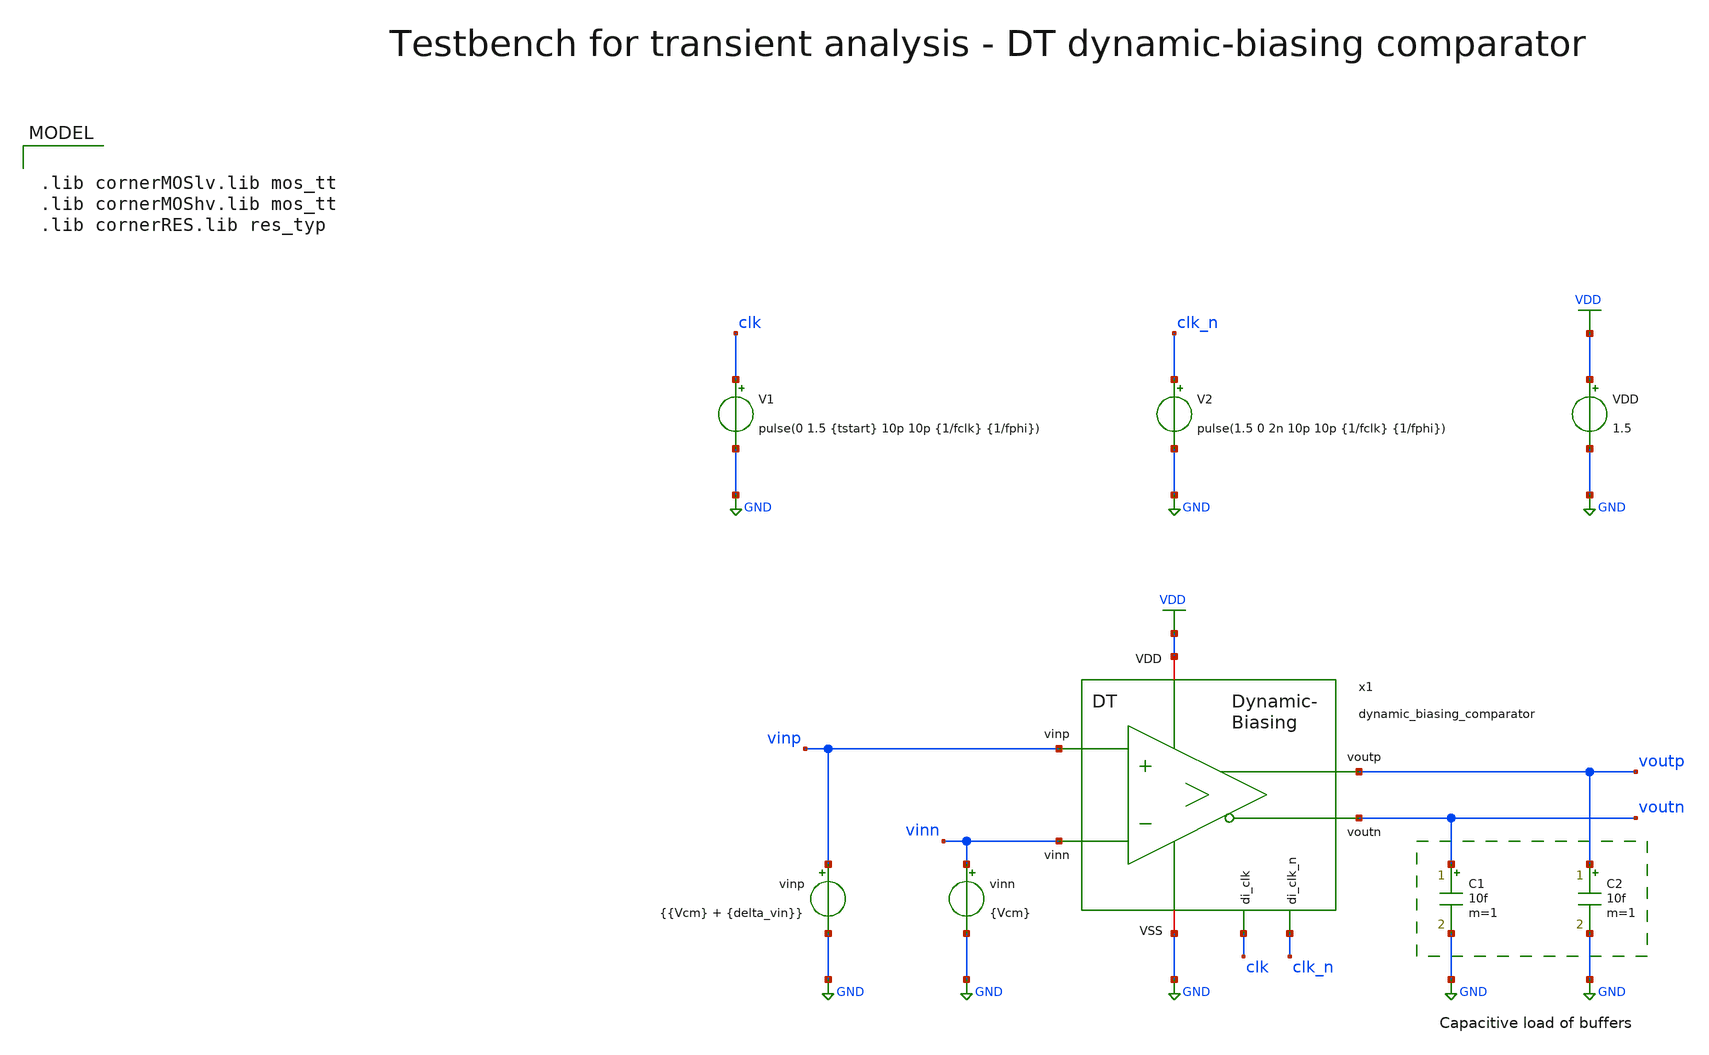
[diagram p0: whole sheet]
** sch_path: SG13G2_ATBS-ADC-main/xschem/comparator/discrete_time/Dynamic-biasing/testbenches/dynamic_biasing_comparator_tb_tran.sch
**.subckt dynamic_biasing_comparator_tb_tran
VDD VDD GND 1.5
V1 clk GND pulse(0 1.5 {tstart} 10p 10p {1/fclk} {1/fphi})
vinn vinn GND {Vcm}
vinp vinp GND {{Vcm} + {delta_vin}}
V2 clk_n GND pulse(1.5 0 2n 10p 10p {1/fclk} {1/fphi})
C1 voutn GND 10f m=1
C2 voutp GND 10f m=1
x1 clk_n clk VDD voutp vinp GND voutn vinn dynamic_biasing_comparator
**** begin user architecture code

.lib cornerMOSlv.lib mos_tt
.lib cornerMOShv.lib mos_tt
.lib cornerRES.lib res_typ



.param temp=27
.param fclk=8000000
.param fphi=62500
.param tstart=2n
.param delta_vin = 10m
.param Vcm=0.75
.csparam fclk=fclk
.csparam tstart=tstart
.options savecurrents reltol=1e-3 abstol=1e-12 gmin=1e-15
.control
save all

* Operating Point Analysis
op
remzerovec
write dynamic_biasing_comparator_tb_tran.raw
set appendwrite

* Transient Analysis
* tran 4p 20n
tran 40p 150n
write dynamic_biasing_comparator_tb_tran.raw

* Measure vcpp_min & vcpn_min
let tmeas = 1/fclk
meas tran vcpp_min FIND v(x1.vcpp) at=tmeas
meas tran vcpn_min FIND v(x1.vcpn) at=tmeas

* Measure Propagation Delay
* Time from clock rising edge to 90% VDD of voutp
let voutp_limit = 0.9 * 1.5
meas tran tcross WHEN v(voutp)=voutp_limit CROSS=1
let tpd = tcross - tstart
echo Propagation Delay $&tpd s

* Calculate Energy / Conversion
* i_int in As
* energy_conv in Ws = J
let N = 1
let t_conv = 150n
meas tran i_int INTEG i(VDD) from=tstart to=t_conv
let energy_conv = 1.5 * i_int / N

let energy_conv_femto = energy_conv * 1e15
echo Energy / Conversion $&energy_conv_femto fJ/conv

* Plotting
plot v(clk) v(x1.vs) v(x1.vctail) v(x1.vcpp) v(x1.vcpn) v(voutp) v(voutn)
plot i(VDD)

* Writing Data
set wr_singlescale
set wr_vecnames
let vs=x1.vs
let vctail=x1.vctail
let vcpp=x1.vcpp
let vcpn=x1.vcpn
wrdata
+ /foss/designs/SG13G2_ATBS-ADC-main/python/plot_simulations/data/dynamic_biasing_comparator_tb_tran.txt v(clk) v(vs) v(vctail) v(vcpp) v(vcpn) v(voutp) v(voutn)

*quit
.endc

**** end user architecture code
**.ends

* expanding   symbol:  comparator/discrete_time/Dynamic-biasing/dynamic_biasing_comparator.sym # of
*+ pins=8
** sym_path: SG13G2_ATBS-ADC-main/xschem/comparator/discrete_time/Dynamic-biasing/dynamic_biasing_comparator.sym
** sch_path: SG13G2_ATBS-ADC-main/xschem/comparator/discrete_time/Dynamic-biasing/dynamic_biasing_comparator.sch
.subckt dynamic_biasing_comparator di_clk_n di_clk VDD voutp vinp VSS voutn vinn
*.iopin VDD
*.opin voutp
*.opin voutn
*.ipin di_clk_n
*.iopin VSS
*.ipin vinp
*.ipin vinn
*.ipin di_clk
XM3a vs di_clk vctail VSS sg13_lv_nmos w=1.0u l=0.13u ng=1 m=1 mm_ok=1
XM12 voutp di_clk_n VSS VSS sg13_lv_nmos w=1.0u l=0.13u ng=1 m=1 mm_ok=1
XM8 net1 voutn VDD VDD sg13_lv_pmos w=2.0u l=0.13u ng=2 m=1 mm_ok=1
XM10 voutp voutn VSS VSS sg13_lv_nmos w=1.0u l=0.13u ng=1 m=1 mm_ok=1
XM11 voutn voutp VSS VSS sg13_lv_nmos w=1.0u l=0.13u ng=1 m=1 mm_ok=1
XM13 voutn di_clk_n VSS VSS sg13_lv_nmos w=1.0u l=0.13u ng=1 m=1 mm_ok=1
CPn vcpn VSS 300f m=1
CPp vcpp VSS 300f m=1
XM9 net2 voutp VDD VDD sg13_lv_pmos w=2.0u l=0.13u ng=2 m=1 mm_ok=1
XM6 voutp vcpn net1 VDD sg13_lv_pmos w=2.0u l=0.13u ng=2 m=1 mm_ok=1
XM7 voutn vcpp net2 VDD sg13_lv_pmos w=2.0u l=0.13u ng=2 m=1 mm_ok=1
CTAIL vctail VSS 600f m=1
XM3b vctail di_clk_n VSS VSS sg13_lv_nmos w=1.0u l=0.13u ng=1 m=1 mm_ok=1
XM1 vcpn vinp vs VSS sg13_lv_nmos w=1.0u l=0.13u ng=1 m=1 mm_ok=1
XM2 vcpp vinn vs VSS sg13_lv_nmos w=1.0u l=0.13u ng=1 m=1 mm_ok=1
XM4 vcpn di_clk VDD VDD sg13_lv_pmos w=1.0u l=0.13u ng=1 m=1 mm_ok=1
XM5 vcpp di_clk VDD VDD sg13_lv_pmos w=1.0u l=0.13u ng=1 m=1 mm_ok=1
.ends

.GLOBAL GND
.GLOBAL VDD
.end
